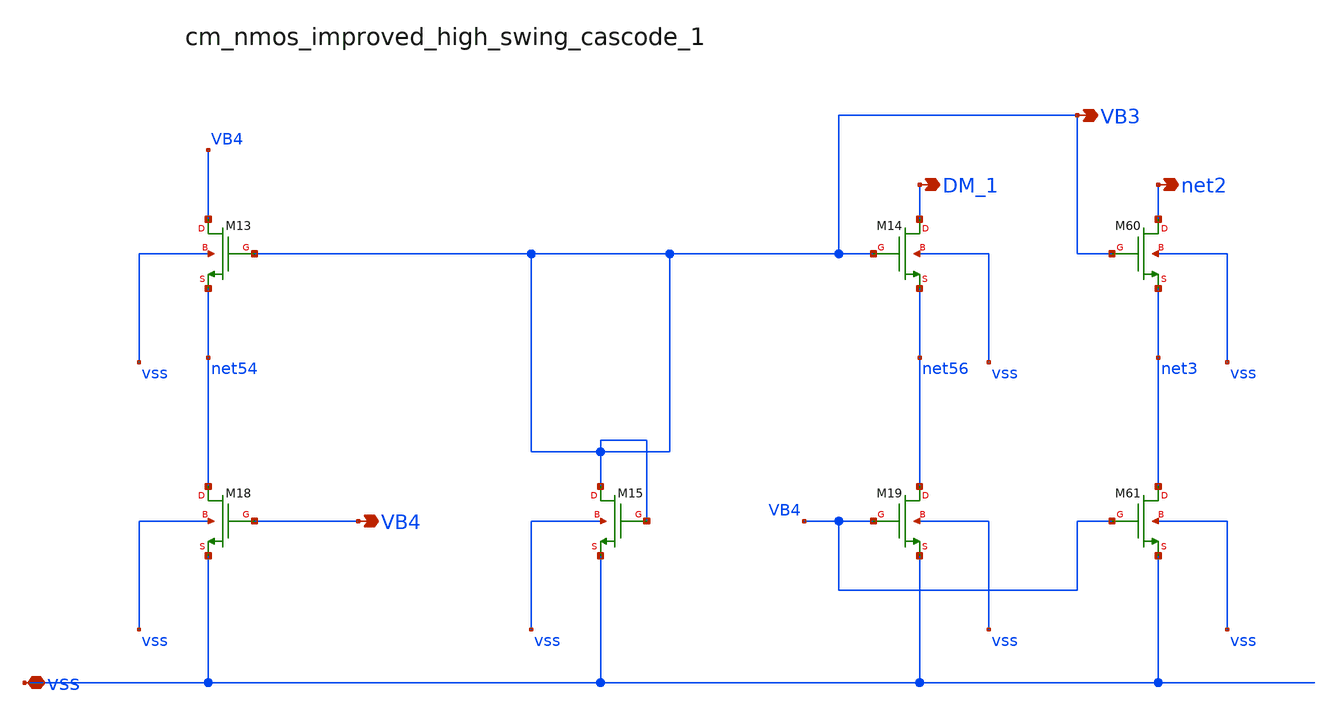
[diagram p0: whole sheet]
** sch_path: analog-db/raw/amp_005_hoilee_affc/hier/blocks/cm_nmos_improved_high_swing_cascode_1.sch
**.subckt cm_nmos_improved_high_swing_cascode_1 vss VB4 DM_1 net2 VB3
*.iopin vss
*.opin VB4
*.opin DM_1
*.opin net2
*.opin VB3
XM13 VB4 VB3 net54 vss sg13_lv_nmos w=x_dut_xm13_w l=x_dut_xm13_l ng=1 m=x_dut_xm13_m
XM14 DM_1 VB3 net56 vss sg13_lv_nmos w=x_dut_xm14_w l=x_dut_xm14_l ng=1 m=x_dut_xm14_m
XM15 VB3 VB3 vss vss sg13_lv_nmos w=x_dut_xm15_w l=x_dut_xm15_l ng=1 m=x_dut_xm15_m
XM18 net54 VB4 vss vss sg13_lv_nmos w=x_dut_xm18_w l=x_dut_xm18_l ng=1 m=x_dut_xm18_m
XM19 net56 VB4 vss vss sg13_lv_nmos w=x_dut_xm19_w l=x_dut_xm19_l ng=1 m=x_dut_xm19_m
XM60 net2 VB3 net3 vss sg13_lv_nmos w=x_dut_xm60_w l=x_dut_xm60_l ng=1 m=x_dut_xm60_m
XM61 net3 VB4 vss vss sg13_lv_nmos w=x_dut_xm61_w l=x_dut_xm61_l ng=1 m=x_dut_xm61_m
**.ends
.end
